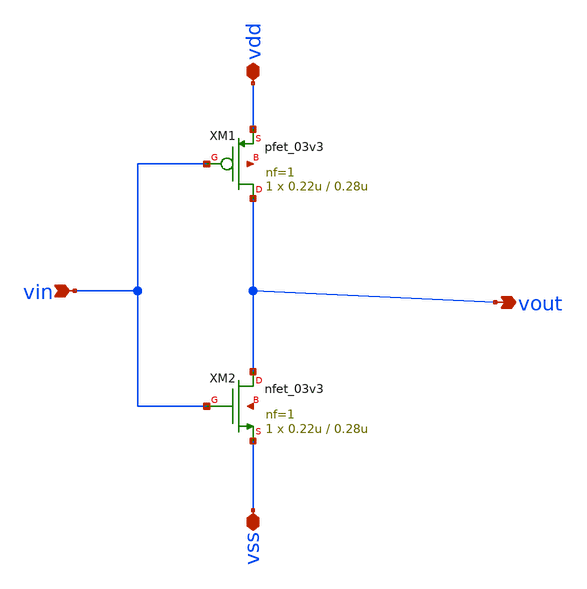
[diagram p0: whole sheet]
** sch_path: designs/inv.sch
**.subckt inv vdd vss vin vout
*.iopin vdd
*.iopin vss
*.ipin vin
*.opin vout
XM1 vout vin vdd net1 pfet_03v3 L=0.28u W=0.22u nf=1 ad='int((nf+1)/2) * W/nf * 0.18u' as='int((nf+2)/2) * W/nf * 0.18u'
+ pd='2*int((nf+1)/2) * (W/nf + 0.18u)' ps='2*int((nf+2)/2) * (W/nf + 0.18u)' nrd='0.18u / W' nrs='0.18u / W'
+ sa=0 sb=0 sd=0 m=1
XM2 vout vin vss net2 nfet_03v3 L=0.28u W=0.22u nf=1 ad='int((nf+1)/2) * W/nf * 0.18u' as='int((nf+2)/2) * W/nf * 0.18u'
+ pd='2*int((nf+1)/2) * (W/nf + 0.18u)' ps='2*int((nf+2)/2) * (W/nf + 0.18u)' nrd='0.18u / W' nrs='0.18u / W'
+ sa=0 sb=0 sd=0 m=1
**.ends
.end
